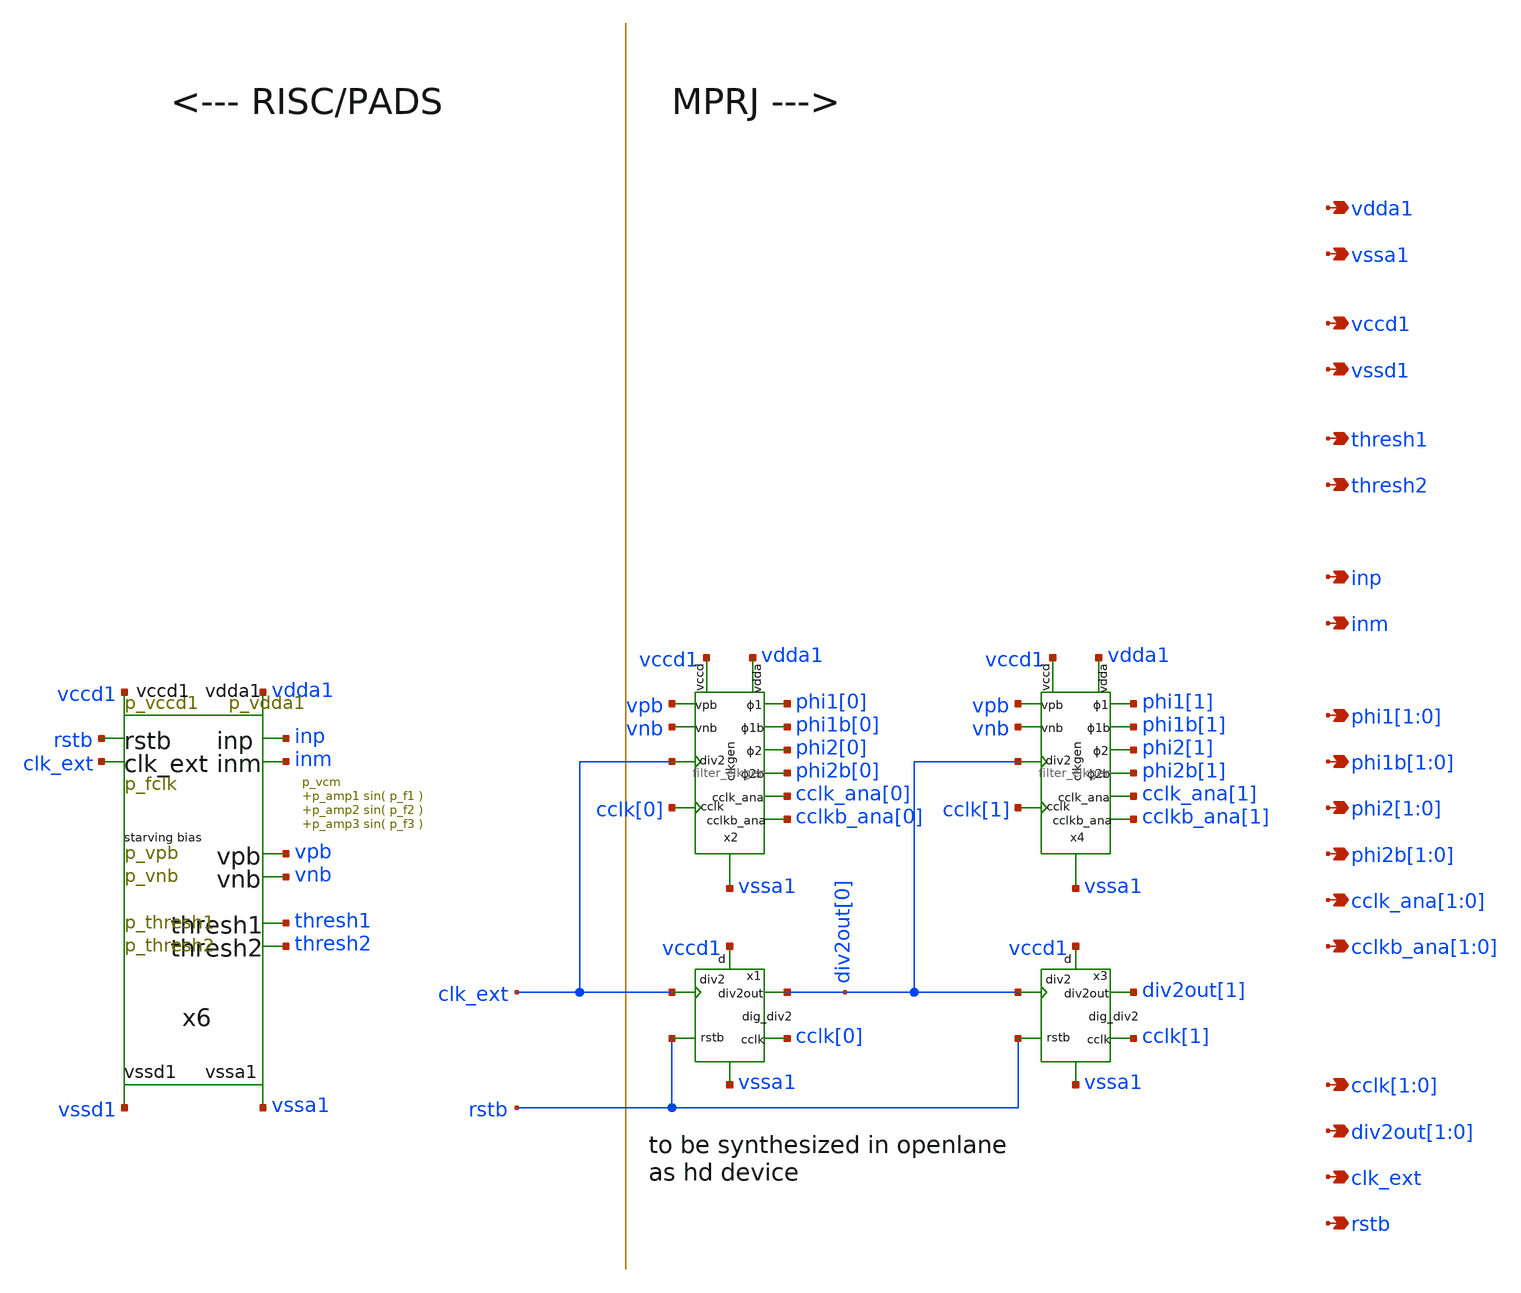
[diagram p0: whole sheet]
** sch_path: xschem/test_bench/risc_signals.sch
**.subckt risc_signals thresh1 thresh2 vdda1 vssa1 inp inm phi1[1],phi1[0] phi1b[1],phi1b[0] vccd1
*+ vssd1 div2out[1],div2out[0] rstb phi2[1],phi2[0] phi2b[1],phi2b[0] cclk_ana[1],cclk_ana[0]
*+ cclkb_ana[1],cclkb_ana[0] clk_ext cclk[1],cclk[0]
*.opin thresh1
*.opin thresh2
*.opin vdda1
*.opin vssa1
*.opin inp
*.opin inm
*.opin phi1[1],phi1[0]
*.opin phi1b[1],phi1b[0]
*.opin vccd1
*.opin vssd1
*.opin div2out[1],div2out[0]
*.opin rstb
*.opin phi2[1],phi2[0]
*.opin phi2b[1],phi2b[0]
*.opin cclk_ana[1],cclk_ana[0]
*.opin cclkb_ana[1],cclkb_ana[0]
*.opin clk_ext
*.opin cclk[1],cclk[0]
x2 cclk[0] phi2b[0] phi2[0] phi1b[0] phi1[0] cclkb_ana[0] cclk_ana[0] vpb vnb vdda1 vssa1 vccd1
+ clk_ext filter_clkgen
x4 cclk[1] phi2b[1] phi2[1] phi1b[1] phi1[1] cclkb_ana[1] cclk_ana[1] vpb vnb vdda1 vssa1 vccd1
+ div2out[0] filter_clkgen
x6 thresh1 thresh2 vdda1 vssa1 inp inm clk_ext rstb vccd1 vssd1 vpb vnb pad_frame p_vdda1=p_vdda1
+ p_vccd1=p_vccd1 p_fclk=p_fclk p_duty_cycle=p_duty_cycle p_rstb_delay=p_rstb_delay p_rstb_tr=p_rstb_tr
+ p_thresh1=p_thresh1 p_thresh2=p_thresh2 p_vpb=p_vpb p_vnb=p_vnb p_vcm=p_vcm p_amp1=p_amp1 p_f1=p_f1 p_amp2=p_amp2
+ p_f2=p_f2 p_amp3=p_amp3 p_f3=p_f3
x1 rstb cclk[0] div2out[0] vccd1 vssa1 clk_ext dig_div2
x3 rstb cclk[1] div2out[1] vccd1 vssa1 div2out[0] dig_div2
**.ends
.end
